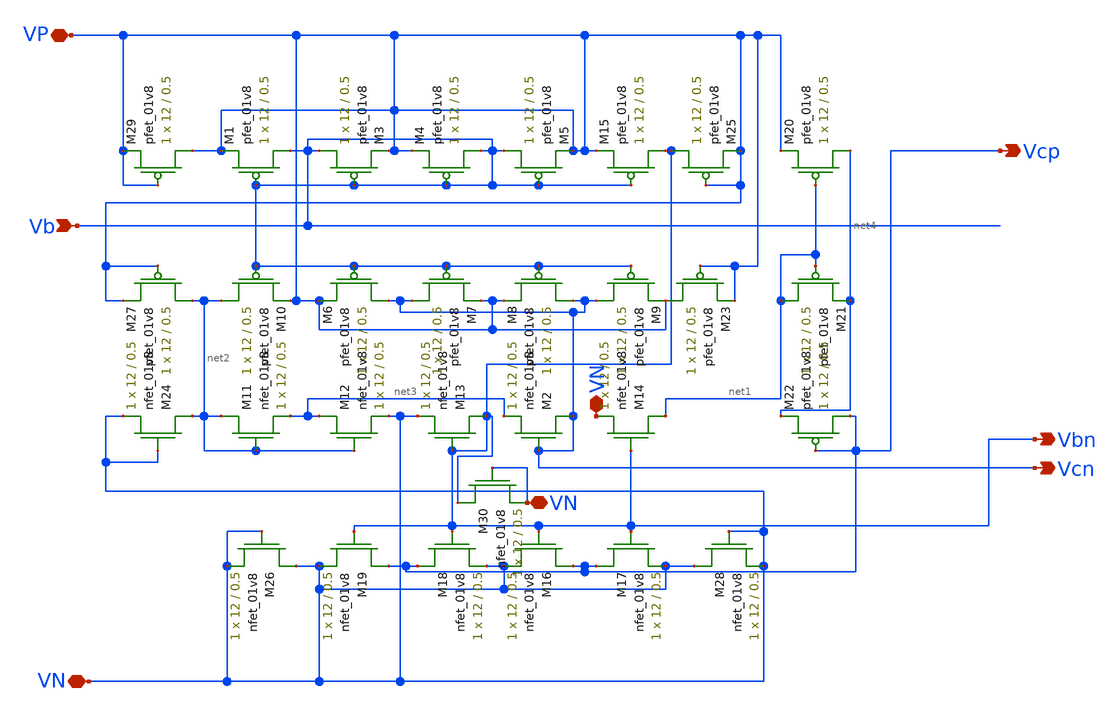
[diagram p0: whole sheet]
** sch_path: MiniProject3-Cascode/XSCHEM/Schematics/VoltageGeneratorLayout.sch
**.subckt VoltageGeneratorLayout VP VN Vcn Vcp Vbn Vb VN VN
*.iopin VP
*.iopin VN
*.opin Vcn
*.opin Vcp
*.opin Vbn
*.ipin Vb
*.iopin VN
*.iopin VN
XM1 Vb Vb VP VP sky130_fd_pr__pfet_01v8 L=0.5 W=12 nf=1 ad='int((nf+1)/2) * W/nf * 0.29' as='int((nf+2)/2) * W/nf * 0.29'
+ pd='2*int((nf+1)/2) * (W/nf + 0.29)' ps='2*int((nf+2)/2) * (W/nf + 0.29)' nrd='0.29 / W' nrs='0.29 / W'
+ sa=0 sb=0 sd=0 mult=1 m=1
XM2 Vcn Vcn net3 VN sky130_fd_pr__nfet_01v8 L=0.5 W=12 nf=1 ad='int((nf+1)/2) * W/nf * 0.29' as='int((nf+2)/2) * W/nf * 0.29'
+ pd='2*int((nf+1)/2) * (W/nf + 0.29)' ps='2*int((nf+2)/2) * (W/nf + 0.29)' nrd='0.29 / W' nrs='0.29 / W'
+ sa=0 sb=0 sd=0 mult=1 m=1
XM3 Vb Vb VP VP sky130_fd_pr__pfet_01v8 L=0.5 W=12 nf=1 ad='int((nf+1)/2) * W/nf * 0.29' as='int((nf+2)/2) * W/nf * 0.29'
+ pd='2*int((nf+1)/2) * (W/nf + 0.29)' ps='2*int((nf+2)/2) * (W/nf + 0.29)' nrd='0.29 / W' nrs='0.29 / W'
+ sa=0 sb=0 sd=0 mult=1 m=1
XM4 Vb Vb VP VP sky130_fd_pr__pfet_01v8 L=0.5 W=12 nf=1 ad='int((nf+1)/2) * W/nf * 0.29' as='int((nf+2)/2) * W/nf * 0.29'
+ pd='2*int((nf+1)/2) * (W/nf + 0.29)' ps='2*int((nf+2)/2) * (W/nf + 0.29)' nrd='0.29 / W' nrs='0.29 / W'
+ sa=0 sb=0 sd=0 mult=1 m=1
XM5 Vb Vb VP VP sky130_fd_pr__pfet_01v8 L=0.5 W=12 nf=1 ad='int((nf+1)/2) * W/nf * 0.29' as='int((nf+2)/2) * W/nf * 0.29'
+ pd='2*int((nf+1)/2) * (W/nf + 0.29)' ps='2*int((nf+2)/2) * (W/nf + 0.29)' nrd='0.29 / W' nrs='0.29 / W'
+ sa=0 sb=0 sd=0 mult=1 m=1
XM6 Vcn Vb VP VP sky130_fd_pr__pfet_01v8 L=0.5 W=12 nf=1 ad='int((nf+1)/2) * W/nf * 0.29' as='int((nf+2)/2) * W/nf * 0.29'
+ pd='2*int((nf+1)/2) * (W/nf + 0.29)' ps='2*int((nf+2)/2) * (W/nf + 0.29)' nrd='0.29 / W' nrs='0.29 / W'
+ sa=0 sb=0 sd=0 mult=1 m=1
XM7 Vcn Vb VP VP sky130_fd_pr__pfet_01v8 L=0.5 W=12 nf=1 ad='int((nf+1)/2) * W/nf * 0.29' as='int((nf+2)/2) * W/nf * 0.29'
+ pd='2*int((nf+1)/2) * (W/nf + 0.29)' ps='2*int((nf+2)/2) * (W/nf + 0.29)' nrd='0.29 / W' nrs='0.29 / W'
+ sa=0 sb=0 sd=0 mult=1 m=1
XM8 Vcn Vb VP VP sky130_fd_pr__pfet_01v8 L=0.5 W=12 nf=1 ad='int((nf+1)/2) * W/nf * 0.29' as='int((nf+2)/2) * W/nf * 0.29'
+ pd='2*int((nf+1)/2) * (W/nf + 0.29)' ps='2*int((nf+2)/2) * (W/nf + 0.29)' nrd='0.29 / W' nrs='0.29 / W'
+ sa=0 sb=0 sd=0 mult=1 m=1
XM9 Vcn Vb VP VP sky130_fd_pr__pfet_01v8 L=0.5 W=12 nf=1 ad='int((nf+1)/2) * W/nf * 0.29' as='int((nf+2)/2) * W/nf * 0.29'
+ pd='2*int((nf+1)/2) * (W/nf + 0.29)' ps='2*int((nf+2)/2) * (W/nf + 0.29)' nrd='0.29 / W' nrs='0.29 / W'
+ sa=0 sb=0 sd=0 mult=1 m=1
XM10 net2 Vb VP VP sky130_fd_pr__pfet_01v8 L=0.5 W=12 nf=1 ad='int((nf+1)/2) * W/nf * 0.29' as='int((nf+2)/2) * W/nf * 0.29'
+ pd='2*int((nf+1)/2) * (W/nf + 0.29)' ps='2*int((nf+2)/2) * (W/nf + 0.29)' nrd='0.29 / W' nrs='0.29 / W'
+ sa=0 sb=0 sd=0 mult=1 m=1
XM11 net2 net2 net3 VN sky130_fd_pr__nfet_01v8 L=0.5 W=12 nf=1 ad='int((nf+1)/2) * W/nf * 0.29' as='int((nf+2)/2) * W/nf * 0.29'
+ pd='2*int((nf+1)/2) * (W/nf + 0.29)' ps='2*int((nf+2)/2) * (W/nf + 0.29)' nrd='0.29 / W' nrs='0.29 / W'
+ sa=0 sb=0 sd=0 mult=1 m=1
XM12 net3 net2 VN VN sky130_fd_pr__nfet_01v8 L=0.5 W=12 nf=1 ad='int((nf+1)/2) * W/nf * 0.29' as='int((nf+2)/2) * W/nf * 0.29'
+ pd='2*int((nf+1)/2) * (W/nf + 0.29)' ps='2*int((nf+2)/2) * (W/nf + 0.29)' nrd='0.29 / W' nrs='0.29 / W'
+ sa=0 sb=0 sd=0 mult=1 m=1
XM13 Vbn Vbn VN VN sky130_fd_pr__nfet_01v8 L=0.5 W=12 nf=1 ad='int((nf+1)/2) * W/nf * 0.29' as='int((nf+2)/2) * W/nf * 0.29'
+ pd='2*int((nf+1)/2) * (W/nf + 0.29)' ps='2*int((nf+2)/2) * (W/nf + 0.29)' nrd='0.29 / W' nrs='0.29 / W'
+ sa=0 sb=0 sd=0 mult=1 m=1
XM14 net1 Vbn VN VN sky130_fd_pr__nfet_01v8 L=0.5 W=12 nf=1 ad='int((nf+1)/2) * W/nf * 0.29' as='int((nf+2)/2) * W/nf * 0.29'
+ pd='2*int((nf+1)/2) * (W/nf + 0.29)' ps='2*int((nf+2)/2) * (W/nf + 0.29)' nrd='0.29 / W' nrs='0.29 / W'
+ sa=0 sb=0 sd=0 mult=1 m=1
XM15 Vbn Vb VP VP sky130_fd_pr__pfet_01v8 L=0.5 W=12 nf=1 ad='int((nf+1)/2) * W/nf * 0.29' as='int((nf+2)/2) * W/nf * 0.29'
+ pd='2*int((nf+1)/2) * (W/nf + 0.29)' ps='2*int((nf+2)/2) * (W/nf + 0.29)' nrd='0.29 / W' nrs='0.29 / W'
+ sa=0 sb=0 sd=0 mult=1 m=1
XM16 Vcp Vbn VN VN sky130_fd_pr__nfet_01v8 L=0.5 W=12 nf=1 ad='int((nf+1)/2) * W/nf * 0.29' as='int((nf+2)/2) * W/nf * 0.29'
+ pd='2*int((nf+1)/2) * (W/nf + 0.29)' ps='2*int((nf+2)/2) * (W/nf + 0.29)' nrd='0.29 / W' nrs='0.29 / W'
+ sa=0 sb=0 sd=0 mult=1 m=1
XM17 Vcp Vbn VN VN sky130_fd_pr__nfet_01v8 L=0.5 W=12 nf=1 ad='int((nf+1)/2) * W/nf * 0.29' as='int((nf+2)/2) * W/nf * 0.29'
+ pd='2*int((nf+1)/2) * (W/nf + 0.29)' ps='2*int((nf+2)/2) * (W/nf + 0.29)' nrd='0.29 / W' nrs='0.29 / W'
+ sa=0 sb=0 sd=0 mult=1 m=1
XM18 Vcp Vbn VN VN sky130_fd_pr__nfet_01v8 L=0.5 W=12 nf=1 ad='int((nf+1)/2) * W/nf * 0.29' as='int((nf+2)/2) * W/nf * 0.29'
+ pd='2*int((nf+1)/2) * (W/nf + 0.29)' ps='2*int((nf+2)/2) * (W/nf + 0.29)' nrd='0.29 / W' nrs='0.29 / W'
+ sa=0 sb=0 sd=0 mult=1 m=1
XM19 Vcp Vbn VN VN sky130_fd_pr__nfet_01v8 L=0.5 W=12 nf=1 ad='int((nf+1)/2) * W/nf * 0.29' as='int((nf+2)/2) * W/nf * 0.29'
+ pd='2*int((nf+1)/2) * (W/nf + 0.29)' ps='2*int((nf+2)/2) * (W/nf + 0.29)' nrd='0.29 / W' nrs='0.29 / W'
+ sa=0 sb=0 sd=0 mult=1 m=1
XM20 net4 net1 VP VP sky130_fd_pr__pfet_01v8 L=0.5 W=12 nf=1 ad='int((nf+1)/2) * W/nf * 0.29' as='int((nf+2)/2) * W/nf * 0.29'
+ pd='2*int((nf+1)/2) * (W/nf + 0.29)' ps='2*int((nf+2)/2) * (W/nf + 0.29)' nrd='0.29 / W' nrs='0.29 / W'
+ sa=0 sb=0 sd=0 mult=1 m=1
XM21 net1 net1 net4 VP sky130_fd_pr__pfet_01v8 L=0.5 W=12 nf=1 ad='int((nf+1)/2) * W/nf * 0.29' as='int((nf+2)/2) * W/nf * 0.29'
+ pd='2*int((nf+1)/2) * (W/nf + 0.29)' ps='2*int((nf+2)/2) * (W/nf + 0.29)' nrd='0.29 / W' nrs='0.29 / W'
+ sa=0 sb=0 sd=0 mult=1 m=1
XM22 Vcp Vcp net4 VP sky130_fd_pr__pfet_01v8 L=0.5 W=12 nf=1 ad='int((nf+1)/2) * W/nf * 0.29' as='int((nf+2)/2) * W/nf * 0.29'
+ pd='2*int((nf+1)/2) * (W/nf + 0.29)' ps='2*int((nf+2)/2) * (W/nf + 0.29)' nrd='0.29 / W' nrs='0.29 / W'
+ sa=0 sb=0 sd=0 mult=1 m=1
XM23 VP VP VP VP sky130_fd_pr__pfet_01v8 L=0.5 W=12 nf=1 ad='int((nf+1)/2) * W/nf * 0.29' as='int((nf+2)/2) * W/nf * 0.29'
+ pd='2*int((nf+1)/2) * (W/nf + 0.29)' ps='2*int((nf+2)/2) * (W/nf + 0.29)' nrd='0.29 / W' nrs='0.29 / W'
+ sa=0 sb=0 sd=0 mult=1 m=1
XM25 Vbn VP VP VP sky130_fd_pr__pfet_01v8 L=0.5 W=12 nf=1 ad='int((nf+1)/2) * W/nf * 0.29' as='int((nf+2)/2) * W/nf * 0.29'
+ pd='2*int((nf+1)/2) * (W/nf + 0.29)' ps='2*int((nf+2)/2) * (W/nf + 0.29)' nrd='0.29 / W' nrs='0.29 / W'
+ sa=0 sb=0 sd=0 mult=1 m=1
XM30 Vbn VN VN VN sky130_fd_pr__nfet_01v8 L=0.5 W=12 nf=1 ad='int((nf+1)/2) * W/nf * 0.29' as='int((nf+2)/2) * W/nf * 0.29'
+ pd='2*int((nf+1)/2) * (W/nf + 0.29)' ps='2*int((nf+2)/2) * (W/nf + 0.29)' nrd='0.29 / W' nrs='0.29 / W'
+ sa=0 sb=0 sd=0 mult=1 m=1
XM26 VN VN VN VN sky130_fd_pr__nfet_01v8 L=0.5 W=12 nf=1 ad='int((nf+1)/2) * W/nf * 0.29' as='int((nf+2)/2) * W/nf * 0.29'
+ pd='2*int((nf+1)/2) * (W/nf + 0.29)' ps='2*int((nf+2)/2) * (W/nf + 0.29)' nrd='0.29 / W' nrs='0.29 / W'
+ sa=0 sb=0 sd=0 mult=1 m=1
XM28 VN VN VN VN sky130_fd_pr__nfet_01v8 L=0.5 W=12 nf=1 ad='int((nf+1)/2) * W/nf * 0.29' as='int((nf+2)/2) * W/nf * 0.29'
+ pd='2*int((nf+1)/2) * (W/nf + 0.29)' ps='2*int((nf+2)/2) * (W/nf + 0.29)' nrd='0.29 / W' nrs='0.29 / W'
+ sa=0 sb=0 sd=0 mult=1 m=1
XM24 net2 VN VN VN sky130_fd_pr__nfet_01v8 L=0.5 W=12 nf=1 ad='int((nf+1)/2) * W/nf * 0.29' as='int((nf+2)/2) * W/nf * 0.29'
+ pd='2*int((nf+1)/2) * (W/nf + 0.29)' ps='2*int((nf+2)/2) * (W/nf + 0.29)' nrd='0.29 / W' nrs='0.29 / W'
+ sa=0 sb=0 sd=0 mult=1 m=1
XM27 net2 VP VP VP sky130_fd_pr__pfet_01v8 L=0.5 W=12 nf=1 ad='int((nf+1)/2) * W/nf * 0.29' as='int((nf+2)/2) * W/nf * 0.29'
+ pd='2*int((nf+1)/2) * (W/nf + 0.29)' ps='2*int((nf+2)/2) * (W/nf + 0.29)' nrd='0.29 / W' nrs='0.29 / W'
+ sa=0 sb=0 sd=0 mult=1 m=1
XM29 VP VP VP VP sky130_fd_pr__pfet_01v8 L=0.5 W=12 nf=1 ad='int((nf+1)/2) * W/nf * 0.29' as='int((nf+2)/2) * W/nf * 0.29'
+ pd='2*int((nf+1)/2) * (W/nf + 0.29)' ps='2*int((nf+2)/2) * (W/nf + 0.29)' nrd='0.29 / W' nrs='0.29 / W'
+ sa=0 sb=0 sd=0 mult=1 m=1
**.ends
.end
